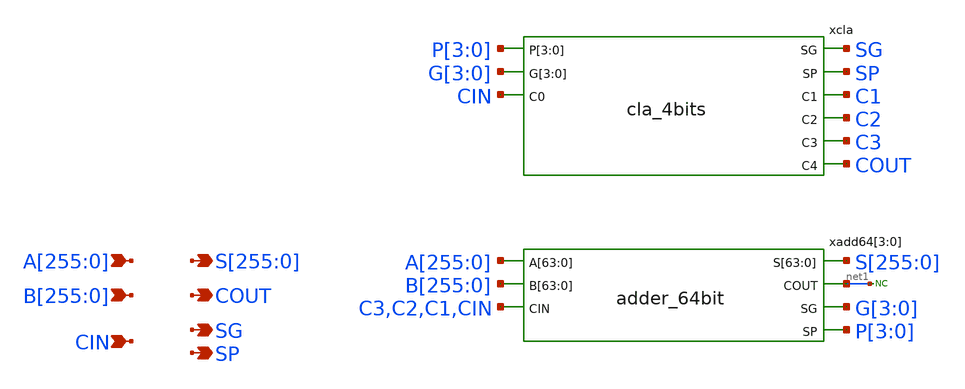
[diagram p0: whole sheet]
** sch_path: sky130A/xschem_libs/sky130_tests/adder_256bit/schematic/adder_256bit.sch
**.subckt adder_256bit
*+ A[255],A[254],A[253],A[252],A[251],A[250],A[249],A[248],A[247],A[246],A[245],A[244],A[243],A[242],A[241],A[240],A[239],A[238],A[237],A[236],A[235],A[234],A[233],A[232],A[231],A[230],A[229],A[228],A[227],A[226],A[225],A[224],A[223],A[222],A[221],A[220],A[219],A[218],A[217],A[216],A[215],A[214],A[213],A[212],A[211],A[210],A[209],A[208],A[207],A[206],A[205],A[204],A[203],A[202],A[201],A[200],A[199],A[198],A[197],A[196],A[195],A[194],A[193],A[192],A[191],A[190],A[189],A[188],A[187],A[186],A[185],A[184],A[183],A[182],A[181],A[180],A[179],A[178],A[177],A[176],A[175],A[174],A[173],A[172],A[171],A[170],A[169],A[168],A[167],A[166],A[165],A[164],A[163],A[162],A[161],A[160],A[159],A[158],A[157],A[156],A[155],A[154],A[153],A[152],A[151],A[150],A[149],A[148],A[147],A[146],A[145],A[144],A[143],A[142],A[141],A[140],A[139],A[138],A[137],A[136],A[135],A[134],A[133],A[132],A[131],A[130],A[129],A[128],A[127],A[126],A[125],A[124],A[123],A[122],A[121],A[120],A[119],A[118],A[117],A[116],A[115],A[114],A[113],A[112],A[111],A[110],A[109],A[108],A[107],A[106],A[105],A[104],A[103],A[102],A[101],A[100],A[99],A[98],A[97],A[96],A[95],A[94],A[93],A[92],A[91],A[90],A[89],A[88],A[87],A[86],A[85],A[84],A[83],A[82],A[81],A[80],A[79],A[78],A[77],A[76],A[75],A[74],A[73],A[72],A[71],A[70],A[69],A[68],A[67],A[66],A[65],A[64],A[63],A[62],A[61],A[60],A[59],A[58],A[57],A[56],A[55],A[54],A[53],A[52],A[51],A[50],A[49],A[48],A[47],A[46],A[45],A[44],A[43],A[42],A[41],A[40],A[39],A[38],A[37],A[36],A[35],A[34],A[33],A[32],A[31],A[30],A[29],A[28],A[27],A[26],A[25],A[24],A[23],A[22],A[21],A[20],A[19],A[18],A[17],A[16],A[15],A[14],A[13],A[12],A[11],A[10],A[9],A[8],A[7],A[6],A[5],A[4],A[3],A[2],A[1],A[0]
*+ B[255],B[254],B[253],B[252],B[251],B[250],B[249],B[248],B[247],B[246],B[245],B[244],B[243],B[242],B[241],B[240],B[239],B[238],B[237],B[236],B[235],B[234],B[233],B[232],B[231],B[230],B[229],B[228],B[227],B[226],B[225],B[224],B[223],B[222],B[221],B[220],B[219],B[218],B[217],B[216],B[215],B[214],B[213],B[212],B[211],B[210],B[209],B[208],B[207],B[206],B[205],B[204],B[203],B[202],B[201],B[200],B[199],B[198],B[197],B[196],B[195],B[194],B[193],B[192],B[191],B[190],B[189],B[188],B[187],B[186],B[185],B[184],B[183],B[182],B[181],B[180],B[179],B[178],B[177],B[176],B[175],B[174],B[173],B[172],B[171],B[170],B[169],B[168],B[167],B[166],B[165],B[164],B[163],B[162],B[161],B[160],B[159],B[158],B[157],B[156],B[155],B[154],B[153],B[152],B[151],B[150],B[149],B[148],B[147],B[146],B[145],B[144],B[143],B[142],B[141],B[140],B[139],B[138],B[137],B[136],B[135],B[134],B[133],B[132],B[131],B[130],B[129],B[128],B[127],B[126],B[125],B[124],B[123],B[122],B[121],B[120],B[119],B[118],B[117],B[116],B[115],B[114],B[113],B[112],B[111],B[110],B[109],B[108],B[107],B[106],B[105],B[104],B[103],B[102],B[101],B[100],B[99],B[98],B[97],B[96],B[95],B[94],B[93],B[92],B[91],B[90],B[89],B[88],B[87],B[86],B[85],B[84],B[83],B[82],B[81],B[80],B[79],B[78],B[77],B[76],B[75],B[74],B[73],B[72],B[71],B[70],B[69],B[68],B[67],B[66],B[65],B[64],B[63],B[62],B[61],B[60],B[59],B[58],B[57],B[56],B[55],B[54],B[53],B[52],B[51],B[50],B[49],B[48],B[47],B[46],B[45],B[44],B[43],B[42],B[41],B[40],B[39],B[38],B[37],B[36],B[35],B[34],B[33],B[32],B[31],B[30],B[29],B[28],B[27],B[26],B[25],B[24],B[23],B[22],B[21],B[20],B[19],B[18],B[17],B[16],B[15],B[14],B[13],B[12],B[11],B[10],B[9],B[8],B[7],B[6],B[5],B[4],B[3],B[2],B[1],B[0] CIN
*+ S[255],S[254],S[253],S[252],S[251],S[250],S[249],S[248],S[247],S[246],S[245],S[244],S[243],S[242],S[241],S[240],S[239],S[238],S[237],S[236],S[235],S[234],S[233],S[232],S[231],S[230],S[229],S[228],S[227],S[226],S[225],S[224],S[223],S[222],S[221],S[220],S[219],S[218],S[217],S[216],S[215],S[214],S[213],S[212],S[211],S[210],S[209],S[208],S[207],S[206],S[205],S[204],S[203],S[202],S[201],S[200],S[199],S[198],S[197],S[196],S[195],S[194],S[193],S[192],S[191],S[190],S[189],S[188],S[187],S[186],S[185],S[184],S[183],S[182],S[181],S[180],S[179],S[178],S[177],S[176],S[175],S[174],S[173],S[172],S[171],S[170],S[169],S[168],S[167],S[166],S[165],S[164],S[163],S[162],S[161],S[160],S[159],S[158],S[157],S[156],S[155],S[154],S[153],S[152],S[151],S[150],S[149],S[148],S[147],S[146],S[145],S[144],S[143],S[142],S[141],S[140],S[139],S[138],S[137],S[136],S[135],S[134],S[133],S[132],S[131],S[130],S[129],S[128],S[127],S[126],S[125],S[124],S[123],S[122],S[121],S[120],S[119],S[118],S[117],S[116],S[115],S[114],S[113],S[112],S[111],S[110],S[109],S[108],S[107],S[106],S[105],S[104],S[103],S[102],S[101],S[100],S[99],S[98],S[97],S[96],S[95],S[94],S[93],S[92],S[91],S[90],S[89],S[88],S[87],S[86],S[85],S[84],S[83],S[82],S[81],S[80],S[79],S[78],S[77],S[76],S[75],S[74],S[73],S[72],S[71],S[70],S[69],S[68],S[67],S[66],S[65],S[64],S[63],S[62],S[61],S[60],S[59],S[58],S[57],S[56],S[55],S[54],S[53],S[52],S[51],S[50],S[49],S[48],S[47],S[46],S[45],S[44],S[43],S[42],S[41],S[40],S[39],S[38],S[37],S[36],S[35],S[34],S[33],S[32],S[31],S[30],S[29],S[28],S[27],S[26],S[25],S[24],S[23],S[22],S[21],S[20],S[19],S[18],S[17],S[16],S[15],S[14],S[13],S[12],S[11],S[10],S[9],S[8],S[7],S[6],S[5],S[4],S[3],S[2],S[1],S[0] COUT SP SG
*.ipin
*+ A[255],A[254],A[253],A[252],A[251],A[250],A[249],A[248],A[247],A[246],A[245],A[244],A[243],A[242],A[241],A[240],A[239],A[238],A[237],A[236],A[235],A[234],A[233],A[232],A[231],A[230],A[229],A[228],A[227],A[226],A[225],A[224],A[223],A[222],A[221],A[220],A[219],A[218],A[217],A[216],A[215],A[214],A[213],A[212],A[211],A[210],A[209],A[208],A[207],A[206],A[205],A[204],A[203],A[202],A[201],A[200],A[199],A[198],A[197],A[196],A[195],A[194],A[193],A[192],A[191],A[190],A[189],A[188],A[187],A[186],A[185],A[184],A[183],A[182],A[181],A[180],A[179],A[178],A[177],A[176],A[175],A[174],A[173],A[172],A[171],A[170],A[169],A[168],A[167],A[166],A[165],A[164],A[163],A[162],A[161],A[160],A[159],A[158],A[157],A[156],A[155],A[154],A[153],A[152],A[151],A[150],A[149],A[148],A[147],A[146],A[145],A[144],A[143],A[142],A[141],A[140],A[139],A[138],A[137],A[136],A[135],A[134],A[133],A[132],A[131],A[130],A[129],A[128],A[127],A[126],A[125],A[124],A[123],A[122],A[121],A[120],A[119],A[118],A[117],A[116],A[115],A[114],A[113],A[112],A[111],A[110],A[109],A[108],A[107],A[106],A[105],A[104],A[103],A[102],A[101],A[100],A[99],A[98],A[97],A[96],A[95],A[94],A[93],A[92],A[91],A[90],A[89],A[88],A[87],A[86],A[85],A[84],A[83],A[82],A[81],A[80],A[79],A[78],A[77],A[76],A[75],A[74],A[73],A[72],A[71],A[70],A[69],A[68],A[67],A[66],A[65],A[64],A[63],A[62],A[61],A[60],A[59],A[58],A[57],A[56],A[55],A[54],A[53],A[52],A[51],A[50],A[49],A[48],A[47],A[46],A[45],A[44],A[43],A[42],A[41],A[40],A[39],A[38],A[37],A[36],A[35],A[34],A[33],A[32],A[31],A[30],A[29],A[28],A[27],A[26],A[25],A[24],A[23],A[22],A[21],A[20],A[19],A[18],A[17],A[16],A[15],A[14],A[13],A[12],A[11],A[10],A[9],A[8],A[7],A[6],A[5],A[4],A[3],A[2],A[1],A[0]
*.ipin
*+ B[255],B[254],B[253],B[252],B[251],B[250],B[249],B[248],B[247],B[246],B[245],B[244],B[243],B[242],B[241],B[240],B[239],B[238],B[237],B[236],B[235],B[234],B[233],B[232],B[231],B[230],B[229],B[228],B[227],B[226],B[225],B[224],B[223],B[222],B[221],B[220],B[219],B[218],B[217],B[216],B[215],B[214],B[213],B[212],B[211],B[210],B[209],B[208],B[207],B[206],B[205],B[204],B[203],B[202],B[201],B[200],B[199],B[198],B[197],B[196],B[195],B[194],B[193],B[192],B[191],B[190],B[189],B[188],B[187],B[186],B[185],B[184],B[183],B[182],B[181],B[180],B[179],B[178],B[177],B[176],B[175],B[174],B[173],B[172],B[171],B[170],B[169],B[168],B[167],B[166],B[165],B[164],B[163],B[162],B[161],B[160],B[159],B[158],B[157],B[156],B[155],B[154],B[153],B[152],B[151],B[150],B[149],B[148],B[147],B[146],B[145],B[144],B[143],B[142],B[141],B[140],B[139],B[138],B[137],B[136],B[135],B[134],B[133],B[132],B[131],B[130],B[129],B[128],B[127],B[126],B[125],B[124],B[123],B[122],B[121],B[120],B[119],B[118],B[117],B[116],B[115],B[114],B[113],B[112],B[111],B[110],B[109],B[108],B[107],B[106],B[105],B[104],B[103],B[102],B[101],B[100],B[99],B[98],B[97],B[96],B[95],B[94],B[93],B[92],B[91],B[90],B[89],B[88],B[87],B[86],B[85],B[84],B[83],B[82],B[81],B[80],B[79],B[78],B[77],B[76],B[75],B[74],B[73],B[72],B[71],B[70],B[69],B[68],B[67],B[66],B[65],B[64],B[63],B[62],B[61],B[60],B[59],B[58],B[57],B[56],B[55],B[54],B[53],B[52],B[51],B[50],B[49],B[48],B[47],B[46],B[45],B[44],B[43],B[42],B[41],B[40],B[39],B[38],B[37],B[36],B[35],B[34],B[33],B[32],B[31],B[30],B[29],B[28],B[27],B[26],B[25],B[24],B[23],B[22],B[21],B[20],B[19],B[18],B[17],B[16],B[15],B[14],B[13],B[12],B[11],B[10],B[9],B[8],B[7],B[6],B[5],B[4],B[3],B[2],B[1],B[0]
*.ipin CIN
*.opin
*+ S[255],S[254],S[253],S[252],S[251],S[250],S[249],S[248],S[247],S[246],S[245],S[244],S[243],S[242],S[241],S[240],S[239],S[238],S[237],S[236],S[235],S[234],S[233],S[232],S[231],S[230],S[229],S[228],S[227],S[226],S[225],S[224],S[223],S[222],S[221],S[220],S[219],S[218],S[217],S[216],S[215],S[214],S[213],S[212],S[211],S[210],S[209],S[208],S[207],S[206],S[205],S[204],S[203],S[202],S[201],S[200],S[199],S[198],S[197],S[196],S[195],S[194],S[193],S[192],S[191],S[190],S[189],S[188],S[187],S[186],S[185],S[184],S[183],S[182],S[181],S[180],S[179],S[178],S[177],S[176],S[175],S[174],S[173],S[172],S[171],S[170],S[169],S[168],S[167],S[166],S[165],S[164],S[163],S[162],S[161],S[160],S[159],S[158],S[157],S[156],S[155],S[154],S[153],S[152],S[151],S[150],S[149],S[148],S[147],S[146],S[145],S[144],S[143],S[142],S[141],S[140],S[139],S[138],S[137],S[136],S[135],S[134],S[133],S[132],S[131],S[130],S[129],S[128],S[127],S[126],S[125],S[124],S[123],S[122],S[121],S[120],S[119],S[118],S[117],S[116],S[115],S[114],S[113],S[112],S[111],S[110],S[109],S[108],S[107],S[106],S[105],S[104],S[103],S[102],S[101],S[100],S[99],S[98],S[97],S[96],S[95],S[94],S[93],S[92],S[91],S[90],S[89],S[88],S[87],S[86],S[85],S[84],S[83],S[82],S[81],S[80],S[79],S[78],S[77],S[76],S[75],S[74],S[73],S[72],S[71],S[70],S[69],S[68],S[67],S[66],S[65],S[64],S[63],S[62],S[61],S[60],S[59],S[58],S[57],S[56],S[55],S[54],S[53],S[52],S[51],S[50],S[49],S[48],S[47],S[46],S[45],S[44],S[43],S[42],S[41],S[40],S[39],S[38],S[37],S[36],S[35],S[34],S[33],S[32],S[31],S[30],S[29],S[28],S[27],S[26],S[25],S[24],S[23],S[22],S[21],S[20],S[19],S[18],S[17],S[16],S[15],S[14],S[13],S[12],S[11],S[10],S[9],S[8],S[7],S[6],S[5],S[4],S[3],S[2],S[1],S[0]
*.opin COUT
*.opin SP
*.opin SG
xadd64[3] A[255] A[254] A[253] A[252] A[251] A[250] A[249] A[248] A[247] A[246] A[245] A[244] A[243]
+ A[242] A[241] A[240] A[239] A[238] A[237] A[236] A[235] A[234] A[233] A[232] A[231] A[230] A[229] A[228]
+ A[227] A[226] A[225] A[224] A[223] A[222] A[221] A[220] A[219] A[218] A[217] A[216] A[215] A[214] A[213]
+ A[212] A[211] A[210] A[209] A[208] A[207] A[206] A[205] A[204] A[203] A[202] A[201] A[200] A[199] A[198]
+ A[197] A[196] A[195] A[194] A[193] A[192] S[255] S[254] S[253] S[252] S[251] S[250] S[249] S[248] S[247]
+ S[246] S[245] S[244] S[243] S[242] S[241] S[240] S[239] S[238] S[237] S[236] S[235] S[234] S[233] S[232]
+ S[231] S[230] S[229] S[228] S[227] S[226] S[225] S[224] S[223] S[222] S[221] S[220] S[219] S[218] S[217]
+ S[216] S[215] S[214] S[213] S[212] S[211] S[210] S[209] S[208] S[207] S[206] S[205] S[204] S[203] S[202]
+ S[201] S[200] S[199] S[198] S[197] S[196] S[195] S[194] S[193] S[192] B[255] B[254] B[253] B[252] B[251]
+ B[250] B[249] B[248] B[247] B[246] B[245] B[244] B[243] B[242] B[241] B[240] B[239] B[238] B[237] B[236]
+ B[235] B[234] B[233] B[232] B[231] B[230] B[229] B[228] B[227] B[226] B[225] B[224] B[223] B[222] B[221]
+ B[220] B[219] B[218] B[217] B[216] B[215] B[214] B[213] B[212] B[211] B[210] B[209] B[208] B[207] B[206]
+ B[205] B[204] B[203] B[202] B[201] B[200] B[199] B[198] B[197] B[196] B[195] B[194] B[193] B[192] net1
+ G[3] C3 P[3] adder_64bit
xadd64[2] A[191] A[190] A[189] A[188] A[187] A[186] A[185] A[184] A[183] A[182] A[181] A[180] A[179]
+ A[178] A[177] A[176] A[175] A[174] A[173] A[172] A[171] A[170] A[169] A[168] A[167] A[166] A[165] A[164]
+ A[163] A[162] A[161] A[160] A[159] A[158] A[157] A[156] A[155] A[154] A[153] A[152] A[151] A[150] A[149]
+ A[148] A[147] A[146] A[145] A[144] A[143] A[142] A[141] A[140] A[139] A[138] A[137] A[136] A[135] A[134]
+ A[133] A[132] A[131] A[130] A[129] A[128] S[191] S[190] S[189] S[188] S[187] S[186] S[185] S[184] S[183]
+ S[182] S[181] S[180] S[179] S[178] S[177] S[176] S[175] S[174] S[173] S[172] S[171] S[170] S[169] S[168]
+ S[167] S[166] S[165] S[164] S[163] S[162] S[161] S[160] S[159] S[158] S[157] S[156] S[155] S[154] S[153]
+ S[152] S[151] S[150] S[149] S[148] S[147] S[146] S[145] S[144] S[143] S[142] S[141] S[140] S[139] S[138]
+ S[137] S[136] S[135] S[134] S[133] S[132] S[131] S[130] S[129] S[128] B[191] B[190] B[189] B[188] B[187]
+ B[186] B[185] B[184] B[183] B[182] B[181] B[180] B[179] B[178] B[177] B[176] B[175] B[174] B[173] B[172]
+ B[171] B[170] B[169] B[168] B[167] B[166] B[165] B[164] B[163] B[162] B[161] B[160] B[159] B[158] B[157]
+ B[156] B[155] B[154] B[153] B[152] B[151] B[150] B[149] B[148] B[147] B[146] B[145] B[144] B[143] B[142]
+ B[141] B[140] B[139] B[138] B[137] B[136] B[135] B[134] B[133] B[132] B[131] B[130] B[129] B[128] net1
+ G[2] C2 P[2] adder_64bit
xadd64[1] A[127] A[126] A[125] A[124] A[123] A[122] A[121] A[120] A[119] A[118] A[117] A[116] A[115]
+ A[114] A[113] A[112] A[111] A[110] A[109] A[108] A[107] A[106] A[105] A[104] A[103] A[102] A[101] A[100]
+ A[99] A[98] A[97] A[96] A[95] A[94] A[93] A[92] A[91] A[90] A[89] A[88] A[87] A[86] A[85] A[84] A[83]
+ A[82] A[81] A[80] A[79] A[78] A[77] A[76] A[75] A[74] A[73] A[72] A[71] A[70] A[69] A[68] A[67] A[66]
+ A[65] A[64] S[127] S[126] S[125] S[124] S[123] S[122] S[121] S[120] S[119] S[118] S[117] S[116] S[115]
+ S[114] S[113] S[112] S[111] S[110] S[109] S[108] S[107] S[106] S[105] S[104] S[103] S[102] S[101] S[100]
+ S[99] S[98] S[97] S[96] S[95] S[94] S[93] S[92] S[91] S[90] S[89] S[88] S[87] S[86] S[85] S[84] S[83]
+ S[82] S[81] S[80] S[79] S[78] S[77] S[76] S[75] S[74] S[73] S[72] S[71] S[70] S[69] S[68] S[67] S[66]
+ S[65] S[64] B[127] B[126] B[125] B[124] B[123] B[122] B[121] B[120] B[119] B[118] B[117] B[116] B[115]
+ B[114] B[113] B[112] B[111] B[110] B[109] B[108] B[107] B[106] B[105] B[104] B[103] B[102] B[101] B[100]
+ B[99] B[98] B[97] B[96] B[95] B[94] B[93] B[92] B[91] B[90] B[89] B[88] B[87] B[86] B[85] B[84] B[83]
+ B[82] B[81] B[80] B[79] B[78] B[77] B[76] B[75] B[74] B[73] B[72] B[71] B[70] B[69] B[68] B[67] B[66]
+ B[65] B[64] net1 G[1] C1 P[1] adder_64bit
xadd64[0] A[63] A[62] A[61] A[60] A[59] A[58] A[57] A[56] A[55] A[54] A[53] A[52] A[51] A[50] A[49]
+ A[48] A[47] A[46] A[45] A[44] A[43] A[42] A[41] A[40] A[39] A[38] A[37] A[36] A[35] A[34] A[33] A[32]
+ A[31] A[30] A[29] A[28] A[27] A[26] A[25] A[24] A[23] A[22] A[21] A[20] A[19] A[18] A[17] A[16] A[15]
+ A[14] A[13] A[12] A[11] A[10] A[9] A[8] A[7] A[6] A[5] A[4] A[3] A[2] A[1] A[0] S[63] S[62] S[61] S[60]
+ S[59] S[58] S[57] S[56] S[55] S[54] S[53] S[52] S[51] S[50] S[49] S[48] S[47] S[46] S[45] S[44] S[43]
+ S[42] S[41] S[40] S[39] S[38] S[37] S[36] S[35] S[34] S[33] S[32] S[31] S[30] S[29] S[28] S[27] S[26]
+ S[25] S[24] S[23] S[22] S[21] S[20] S[19] S[18] S[17] S[16] S[15] S[14] S[13] S[12] S[11] S[10] S[9] S[8]
+ S[7] S[6] S[5] S[4] S[3] S[2] S[1] S[0] B[63] B[62] B[61] B[60] B[59] B[58] B[57] B[56] B[55] B[54]
+ B[53] B[52] B[51] B[50] B[49] B[48] B[47] B[46] B[45] B[44] B[43] B[42] B[41] B[40] B[39] B[38] B[37]
+ B[36] B[35] B[34] B[33] B[32] B[31] B[30] B[29] B[28] B[27] B[26] B[25] B[24] B[23] B[22] B[21] B[20]
+ B[19] B[18] B[17] B[16] B[15] B[14] B[13] B[12] B[11] B[10] B[9] B[8] B[7] B[6] B[5] B[4] B[3] B[2] B[1]
+ B[0] net1 G[0] CIN P[0] adder_64bit
xcla SG SP C1 P[3] P[2] P[1] P[0] C2 G[3] G[2] G[1] G[0] C3 COUT CIN cla_4bits
* noconn #net1
**.ends

* expanding   symbol:  sky130_tests/adder_64bit.sym # of pins=7
** sym_path: sky130_tests/adder_64bit.sym
** sch_path: sky130_tests/adder_64bit.sch
.subckt adder_64bit A[63] A[62] A[61] A[60] A[59] A[58] A[57] A[56] A[55] A[54] A[53] A[52] A[51]
+ A[50] A[49] A[48] A[47] A[46] A[45] A[44] A[43] A[42] A[41] A[40] A[39] A[38] A[37] A[36] A[35] A[34]
+ A[33] A[32] A[31] A[30] A[29] A[28] A[27] A[26] A[25] A[24] A[23] A[22] A[21] A[20] A[19] A[18] A[17]
+ A[16] A[15] A[14] A[13] A[12] A[11] A[10] A[9] A[8] A[7] A[6] A[5] A[4] A[3] A[2] A[1] A[0] S[63] S[62]
+ S[61] S[60] S[59] S[58] S[57] S[56] S[55] S[54] S[53] S[52] S[51] S[50] S[49] S[48] S[47] S[46] S[45]
+ S[44] S[43] S[42] S[41] S[40] S[39] S[38] S[37] S[36] S[35] S[34] S[33] S[32] S[31] S[30] S[29] S[28]
+ S[27] S[26] S[25] S[24] S[23] S[22] S[21] S[20] S[19] S[18] S[17] S[16] S[15] S[14] S[13] S[12] S[11]
+ S[10] S[9] S[8] S[7] S[6] S[5] S[4] S[3] S[2] S[1] S[0] B[63] B[62] B[61] B[60] B[59] B[58] B[57] B[56]
+ B[55] B[54] B[53] B[52] B[51] B[50] B[49] B[48] B[47] B[46] B[45] B[44] B[43] B[42] B[41] B[40] B[39]
+ B[38] B[37] B[36] B[35] B[34] B[33] B[32] B[31] B[30] B[29] B[28] B[27] B[26] B[25] B[24] B[23] B[22]
+ B[21] B[20] B[19] B[18] B[17] B[16] B[15] B[14] B[13] B[12] B[11] B[10] B[9] B[8] B[7] B[6] B[5] B[4]
+ B[3] B[2] B[1] B[0] COUT SG CIN SP
*.ipin
*+ A[63],A[62],A[61],A[60],A[59],A[58],A[57],A[56],A[55],A[54],A[53],A[52],A[51],A[50],A[49],A[48],A[47],A[46],A[45],A[44],A[43],A[42],A[41],A[40],A[39],A[38],A[37],A[36],A[35],A[34],A[33],A[32],A[31],A[30],A[29],A[28],A[27],A[26],A[25],A[24],A[23],A[22],A[21],A[20],A[19],A[18],A[17],A[16],A[15],A[14],A[13],A[12],A[11],A[10],A[9],A[8],A[7],A[6],A[5],A[4],A[3],A[2],A[1],A[0]
*.ipin
*+ B[63],B[62],B[61],B[60],B[59],B[58],B[57],B[56],B[55],B[54],B[53],B[52],B[51],B[50],B[49],B[48],B[47],B[46],B[45],B[44],B[43],B[42],B[41],B[40],B[39],B[38],B[37],B[36],B[35],B[34],B[33],B[32],B[31],B[30],B[29],B[28],B[27],B[26],B[25],B[24],B[23],B[22],B[21],B[20],B[19],B[18],B[17],B[16],B[15],B[14],B[13],B[12],B[11],B[10],B[9],B[8],B[7],B[6],B[5],B[4],B[3],B[2],B[1],B[0]
*.ipin CIN
*.opin
*+ S[63],S[62],S[61],S[60],S[59],S[58],S[57],S[56],S[55],S[54],S[53],S[52],S[51],S[50],S[49],S[48],S[47],S[46],S[45],S[44],S[43],S[42],S[41],S[40],S[39],S[38],S[37],S[36],S[35],S[34],S[33],S[32],S[31],S[30],S[29],S[28],S[27],S[26],S[25],S[24],S[23],S[22],S[21],S[20],S[19],S[18],S[17],S[16],S[15],S[14],S[13],S[12],S[11],S[10],S[9],S[8],S[7],S[6],S[5],S[4],S[3],S[2],S[1],S[0]
*.opin SP
*.opin SG
*.opin COUT
xadd16[3] A[63] A[62] A[61] A[60] A[59] A[58] A[57] A[56] A[55] A[54] A[53] A[52] A[51] A[50] A[49]
+ A[48] S[63] S[62] S[61] S[60] S[59] S[58] S[57] S[56] S[55] S[54] S[53] S[52] S[51] S[50] S[49] S[48]
+ B[63] B[62] B[61] B[60] B[59] B[58] B[57] B[56] B[55] B[54] B[53] B[52] B[51] B[50] B[49] B[48] net1 G[3]
+ C3 P[3] adder_16bit
xadd16[2] A[47] A[46] A[45] A[44] A[43] A[42] A[41] A[40] A[39] A[38] A[37] A[36] A[35] A[34] A[33]
+ A[32] S[47] S[46] S[45] S[44] S[43] S[42] S[41] S[40] S[39] S[38] S[37] S[36] S[35] S[34] S[33] S[32]
+ B[47] B[46] B[45] B[44] B[43] B[42] B[41] B[40] B[39] B[38] B[37] B[36] B[35] B[34] B[33] B[32] net1 G[2]
+ C2 P[2] adder_16bit
xadd16[1] A[31] A[30] A[29] A[28] A[27] A[26] A[25] A[24] A[23] A[22] A[21] A[20] A[19] A[18] A[17]
+ A[16] S[31] S[30] S[29] S[28] S[27] S[26] S[25] S[24] S[23] S[22] S[21] S[20] S[19] S[18] S[17] S[16]
+ B[31] B[30] B[29] B[28] B[27] B[26] B[25] B[24] B[23] B[22] B[21] B[20] B[19] B[18] B[17] B[16] net1 G[1]
+ C1 P[1] adder_16bit
xadd16[0] A[15] A[14] A[13] A[12] A[11] A[10] A[9] A[8] A[7] A[6] A[5] A[4] A[3] A[2] A[1] A[0]
+ S[15] S[14] S[13] S[12] S[11] S[10] S[9] S[8] S[7] S[6] S[5] S[4] S[3] S[2] S[1] S[0] B[15] B[14] B[13]
+ B[12] B[11] B[10] B[9] B[8] B[7] B[6] B[5] B[4] B[3] B[2] B[1] B[0] net1 G[0] CIN P[0] adder_16bit
xcla SG SP C1 P[3] P[2] P[1] P[0] C2 G[3] G[2] G[1] G[0] C3 COUT CIN cla_4bits
* noconn #net1
.ends


* expanding   symbol:  sky130_tests/cla_4bits.sym # of pins=9
** sym_path: sky130_tests/cla_4bits.sym
** sch_path: sky130_tests/cla_4bits.sch
.subckt cla_4bits SG SP C1 P[3] P[2] P[1] P[0] C2 G[3] G[2] G[1] G[0] C3 C4 C0
*.ipin P[3],P[2],P[1],P[0]
*.ipin G[3],G[2],G[1],G[0]
*.ipin C0
*.opin C4
*.opin C3
*.opin C2
*.opin C1
*.opin SG
*.opin SP
x1 P[0] VSS VSS VCC VCC net4 sky130_fd_sc_hd__inv_1
x2 net5 VSS VSS VCC VCC C1 sky130_fd_sc_hd__inv_1
x3 P[1] VSS VSS VCC VCC net2 sky130_fd_sc_hd__inv_1
x4 net8 VSS VSS VCC VCC C3 sky130_fd_sc_hd__inv_1
x5 G[1] VSS VSS VCC VCC net3 sky130_fd_sc_hd__inv_1
x6 net12 VSS VSS VCC VCC net13 sky130_fd_sc_hd__inv_1
x7 G[1] P[2] G[2] VSS VSS VCC VCC net12 sky130_fd_sc_hd__a21oi_1
x8 P[3] net13 G[3] VSS VSS VCC VCC net14 sky130_fd_sc_hd__a21oi_1
x9 C0 P[0] G[0] VSS VSS VCC VCC net5 sky130_fd_sc_hd__a21oi_1
x10 P[2] C2 G[2] VSS VSS VCC VCC net8 sky130_fd_sc_hd__a21oi_1
x11 G[0] VSS VSS VCC VCC net1 sky130_fd_sc_hd__inv_1
x12 net2 net5 net3 VSS VSS VCC VCC C2 sky130_fd_sc_hd__o21ai_1
x13 net5 net10 net14 VSS VSS VCC VCC C4 sky130_fd_sc_hd__o21ai_1
x14 net1 net10 net14 VSS VSS VCC VCC SG sky130_fd_sc_hd__o21ai_1
x15 net4 net10 VSS VSS VCC VCC SP sky130_fd_sc_hd__nor2_1
x16 P[1] P[2] P[3] VSS VSS VCC VCC net10 sky130_fd_sc_hd__nand3_1
C2 net4 0 5f m=1
C1 net10 0 5f m=1
C3 net1 0 5f m=1
C4 net14 0 5f m=1
C5 net2 0 5f m=1
C6 net5 0 5f m=1
C7 net3 0 5f m=1
C8 net8 0 5f m=1
C9 net13 0 5f m=1
C10 net12 0 5f m=1
C19[3] P[3] 0 5f m=1
C19[2] P[2] 0 5f m=1
C19[1] P[1] 0 5f m=1
C19[0] P[0] 0 5f m=1
C18[3] G[3] 0 5f m=1
C18[2] G[2] 0 5f m=1
C18[1] G[1] 0 5f m=1
C18[0] G[0] 0 5f m=1
C17 C0 0 5f m=1
.ends


* expanding   symbol:  sky130_tests/adder_16bit.sym # of pins=7
** sym_path: sky130_tests/adder_16bit.sym
** sch_path: sky130_tests/adder_16bit.sch
.subckt adder_16bit A[15] A[14] A[13] A[12] A[11] A[10] A[9] A[8] A[7] A[6] A[5] A[4] A[3] A[2] A[1]
+ A[0] S[15] S[14] S[13] S[12] S[11] S[10] S[9] S[8] S[7] S[6] S[5] S[4] S[3] S[2] S[1] S[0] B[15] B[14]
+ B[13] B[12] B[11] B[10] B[9] B[8] B[7] B[6] B[5] B[4] B[3] B[2] B[1] B[0] COUT SG CIN SP
*.ipin A[15],A[14],A[13],A[12],A[11],A[10],A[9],A[8],A[7],A[6],A[5],A[4],A[3],A[2],A[1],A[0]
*.ipin B[15],B[14],B[13],B[12],B[11],B[10],B[9],B[8],B[7],B[6],B[5],B[4],B[3],B[2],B[1],B[0]
*.ipin CIN
*.opin S[15],S[14],S[13],S[12],S[11],S[10],S[9],S[8],S[7],S[6],S[5],S[4],S[3],S[2],S[1],S[0]
*.opin SP
*.opin SG
*.opin COUT
xadd4[3] A[15] A[14] A[13] A[12] S[15] S[14] S[13] S[12] B[15] B[14] B[13] B[12] net1 G[3] C3 P[3]
+ adder_4bit
xadd4[2] A[11] A[10] A[9] A[8] S[11] S[10] S[9] S[8] B[11] B[10] B[9] B[8] net1 G[2] C2 P[2]
+ adder_4bit
xadd4[1] A[7] A[6] A[5] A[4] S[7] S[6] S[5] S[4] B[7] B[6] B[5] B[4] net1 G[1] C1 P[1] adder_4bit
xadd4[0] A[3] A[2] A[1] A[0] S[3] S[2] S[1] S[0] B[3] B[2] B[1] B[0] net1 G[0] CIN P[0] adder_4bit
xcla SG SP C1 P[3] P[2] P[1] P[0] C2 G[3] G[2] G[1] G[0] C3 COUT CIN cla_4bits
* noconn #net1
.ends


* expanding   symbol:  sky130_tests/adder_4bit.sym # of pins=7
** sym_path: sky130_tests/adder_4bit.sym
** sch_path: sky130_tests/adder_4bit.sch
.subckt adder_4bit A[3] A[2] A[1] A[0] S[3] S[2] S[1] S[0] B[3] B[2] B[1] B[0] COUT SG CIN SP
*.ipin A[3],A[2],A[1],A[0]
*.ipin B[3],B[2],B[1],B[0]
*.ipin CIN
*.opin S[3],S[2],S[1],S[0]
*.opin SP
*.opin SG
*.opin COUT
xcla SG SP C1 P[3] P[2] P[1] P[0] C2 G[3] G[2] G[1] G[0] C3 COUT CIN cla_4bits
xadd1[3] S[3] A[3] B[3] G[3] C3 P[3] adder_1bit
xadd1[2] S[2] A[2] B[2] G[2] C2 P[2] adder_1bit
xadd1[1] S[1] A[1] B[1] G[1] C1 P[1] adder_1bit
xadd1[0] S[0] A[0] B[0] G[0] CIN P[0] adder_1bit
.ends


* expanding   symbol:  sky130_tests/adder_1bit.sym # of pins=6
** sym_path: sky130_tests/adder_1bit.sym
** sch_path: sky130_tests/adder_1bit.sch
.subckt adder_1bit S A B G CIN P
*.ipin A
*.ipin B
*.ipin CIN
*.opin S
*.opin P
*.opin G
x4 A B VSS VSS VCC VCC G sky130_fd_sc_hd__and2_1
x2 A B VSS VSS VCC VCC P sky130_fd_sc_hd__xor2_1
x3 P CIN VSS VSS VCC VCC S sky130_fd_sc_hd__xor2_1
C1 G 0 5f m=1
C2 P 0 5f m=1
C3 S 0 5f m=1
.ends

.end
